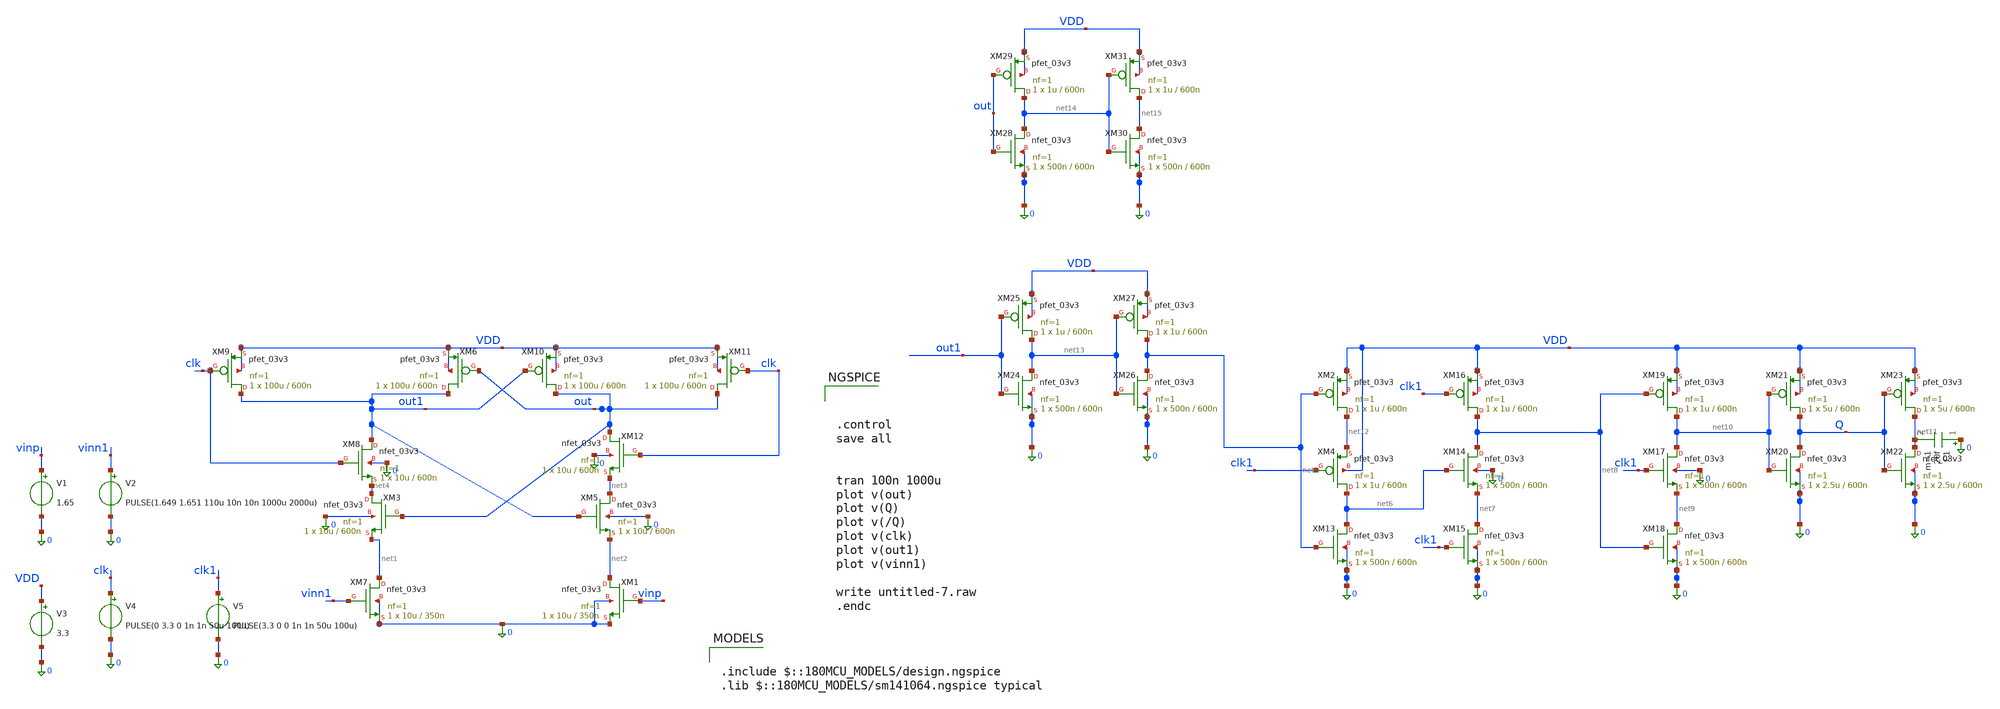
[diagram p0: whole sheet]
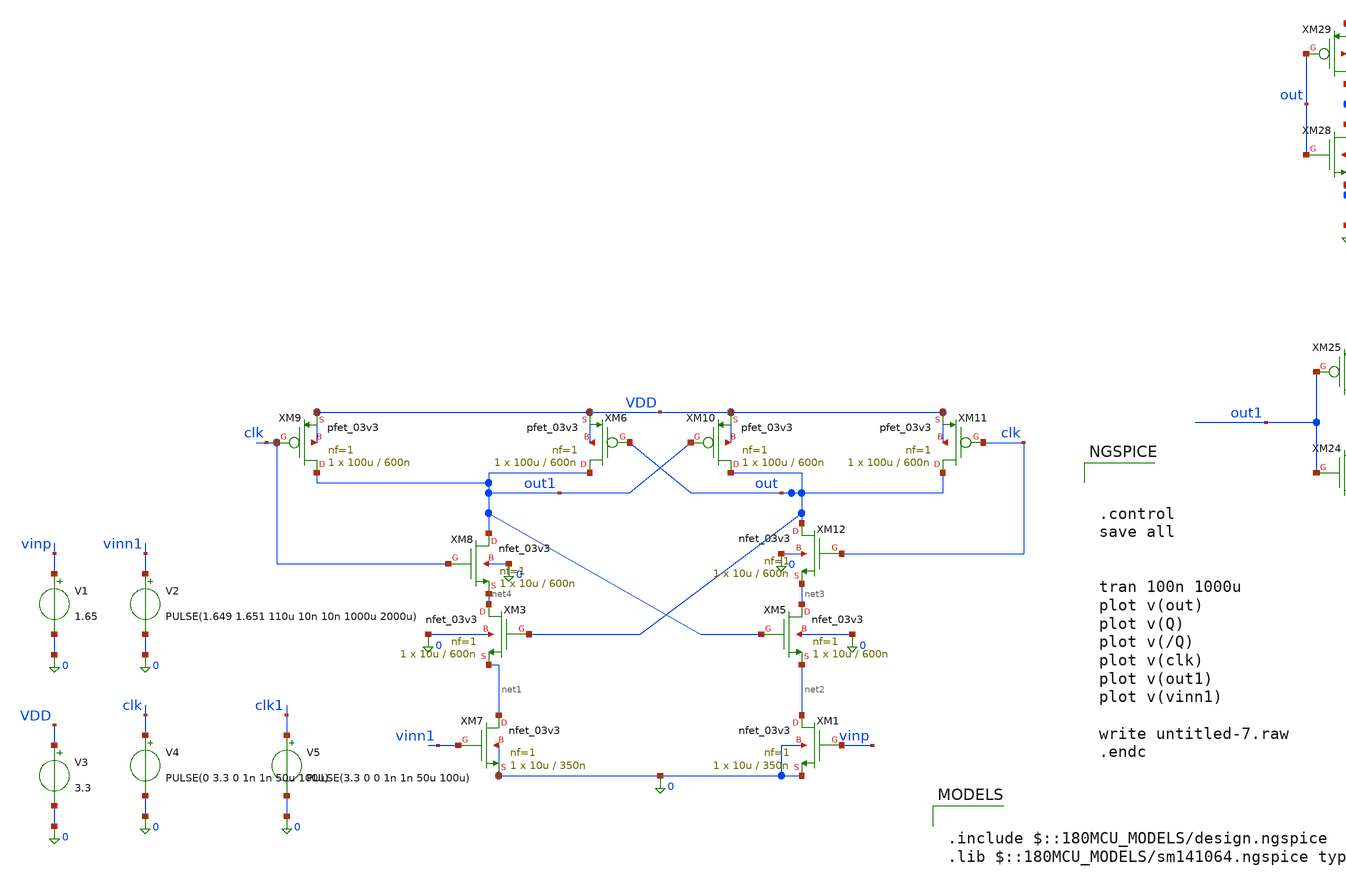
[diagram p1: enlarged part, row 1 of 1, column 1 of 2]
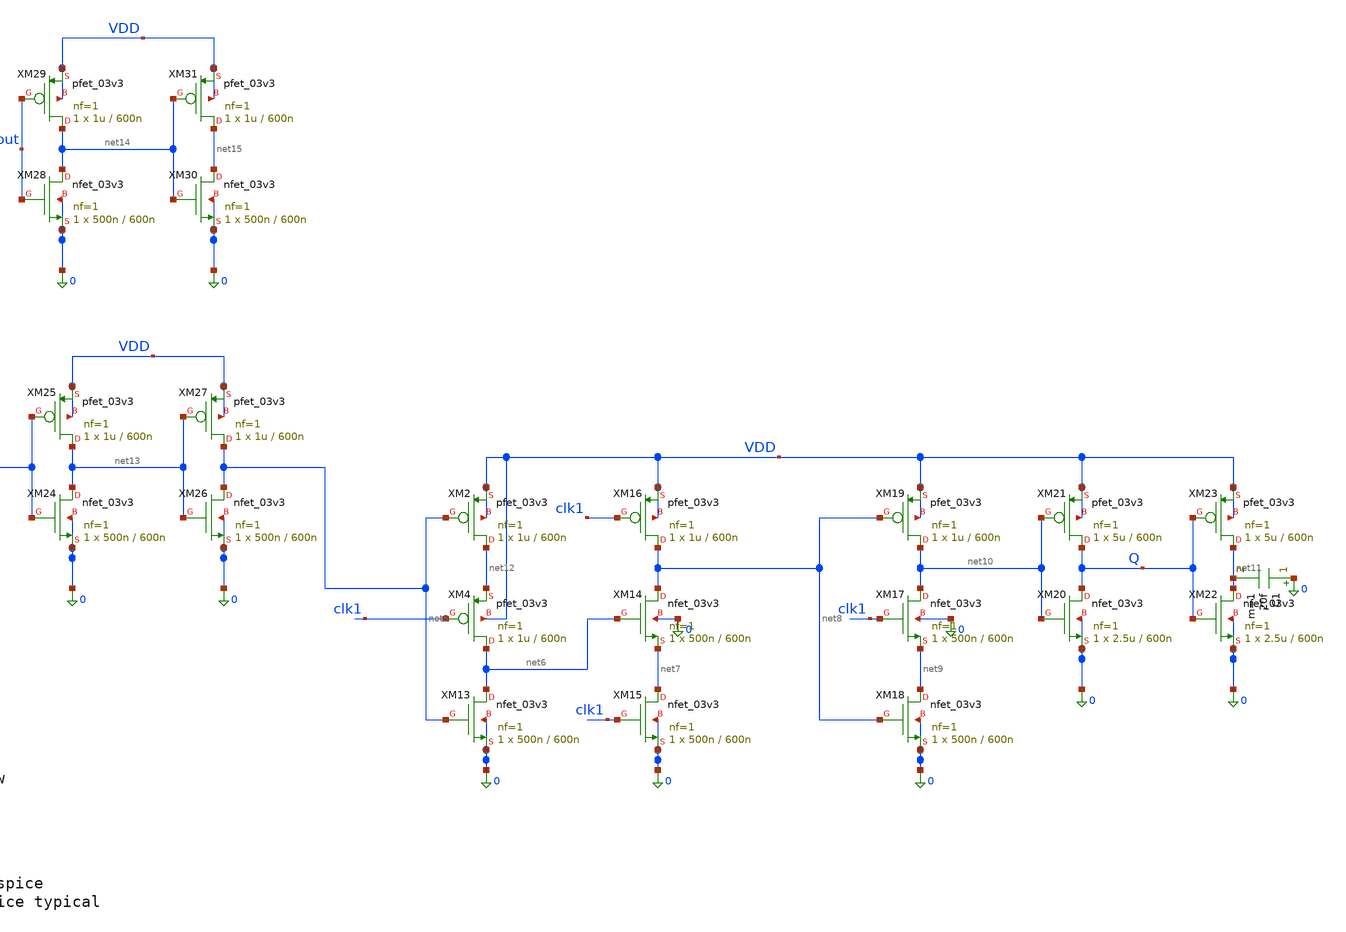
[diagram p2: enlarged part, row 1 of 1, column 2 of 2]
** sch_path: amplifier/untitled-7.sch
**.subckt untitled-7
V1 vinp 0 1.65
V2 vinn1 0 PULSE(1.649 1.651 110u 10n 10n 1000u 2000u)
V3 VDD 0 3.3
XM7 net1 vinn1 0 0 nfet_03v3 L=350n W=10u nf=1 ad='int((nf+1)/2) * W/nf * 0.18u' as='int((nf+2)/2) * W/nf * 0.18u'
+ pd='2*int((nf+1)/2) * (W/nf + 0.18u)' ps='2*int((nf+2)/2) * (W/nf + 0.18u)' nrd='0.18u / W' nrs='0.18u / W'
+ sa=0 sb=0 sd=0 m=1
XM1 net2 vinp 0 0 nfet_03v3 L=350n W=10u nf=1 ad='int((nf+1)/2) * W/nf * 0.18u' as='int((nf+2)/2) * W/nf * 0.18u'
+ pd='2*int((nf+1)/2) * (W/nf + 0.18u)' ps='2*int((nf+2)/2) * (W/nf + 0.18u)' nrd='0.18u / W' nrs='0.18u / W'
+ sa=0 sb=0 sd=0 m=1
XM3 net4 out net1 0 nfet_03v3 L=600n W=10u nf=1 ad='int((nf+1)/2) * W/nf * 0.18u' as='int((nf+2)/2) * W/nf * 0.18u'
+ pd='2*int((nf+1)/2) * (W/nf + 0.18u)' ps='2*int((nf+2)/2) * (W/nf + 0.18u)' nrd='0.18u / W' nrs='0.18u / W'
+ sa=0 sb=0 sd=0 m=1
XM5 net3 out1 net2 0 nfet_03v3 L=600n W=10u nf=1 ad='int((nf+1)/2) * W/nf * 0.18u' as='int((nf+2)/2) * W/nf * 0.18u'
+ pd='2*int((nf+1)/2) * (W/nf + 0.18u)' ps='2*int((nf+2)/2) * (W/nf + 0.18u)' nrd='0.18u / W' nrs='0.18u / W'
+ sa=0 sb=0 sd=0 m=1
V4 clk 0 PULSE(0 3.3 0 1n 1n 50u 100u)
XM6 out1 out VDD VDD pfet_03v3 L=600n W=100u nf=1 ad='int((nf+1)/2) * W/nf * 0.18u' as='int((nf+2)/2) * W/nf * 0.18u'
+ pd='2*int((nf+1)/2) * (W/nf + 0.18u)' ps='2*int((nf+2)/2) * (W/nf + 0.18u)' nrd='0.18u / W' nrs='0.18u / W'
+ sa=0 sb=0 sd=0 m=1
XM10 out out1 VDD VDD pfet_03v3 L=600n W=100u nf=1 ad='int((nf+1)/2) * W/nf * 0.18u' as='int((nf+2)/2) * W/nf * 0.18u'
+ pd='2*int((nf+1)/2) * (W/nf + 0.18u)' ps='2*int((nf+2)/2) * (W/nf + 0.18u)' nrd='0.18u / W' nrs='0.18u / W'
+ sa=0 sb=0 sd=0 m=1
XM9 out1 clk VDD VDD pfet_03v3 L=600n W=100u nf=1 ad='int((nf+1)/2) * W/nf * 0.18u' as='int((nf+2)/2) * W/nf * 0.18u'
+ pd='2*int((nf+1)/2) * (W/nf + 0.18u)' ps='2*int((nf+2)/2) * (W/nf + 0.18u)' nrd='0.18u / W' nrs='0.18u / W'
+ sa=0 sb=0 sd=0 m=1
XM11 out clk VDD VDD pfet_03v3 L=600n W=100u nf=1 ad='int((nf+1)/2) * W/nf * 0.18u' as='int((nf+2)/2) * W/nf * 0.18u'
+ pd='2*int((nf+1)/2) * (W/nf + 0.18u)' ps='2*int((nf+2)/2) * (W/nf + 0.18u)' nrd='0.18u / W' nrs='0.18u / W'
+ sa=0 sb=0 sd=0 m=1
XM8 out1 clk net4 0 nfet_03v3 L=600n W=10u nf=1 ad='int((nf+1)/2) * W/nf * 0.18u' as='int((nf+2)/2) * W/nf * 0.18u'
+ pd='2*int((nf+1)/2) * (W/nf + 0.18u)' ps='2*int((nf+2)/2) * (W/nf + 0.18u)' nrd='0.18u / W' nrs='0.18u / W'
+ sa=0 sb=0 sd=0 m=1
XM12 out clk net3 0 nfet_03v3 L=600n W=10u nf=1 ad='int((nf+1)/2) * W/nf * 0.18u' as='int((nf+2)/2) * W/nf * 0.18u'
+ pd='2*int((nf+1)/2) * (W/nf + 0.18u)' ps='2*int((nf+2)/2) * (W/nf + 0.18u)' nrd='0.18u / W' nrs='0.18u / W'
+ sa=0 sb=0 sd=0 m=1
XM2 net12 net5 VDD VDD pfet_03v3 L=600n W=1u nf=1 ad='int((nf+1)/2) * W/nf * 0.18u' as='int((nf+2)/2) * W/nf * 0.18u'
+ pd='2*int((nf+1)/2) * (W/nf + 0.18u)' ps='2*int((nf+2)/2) * (W/nf + 0.18u)' nrd='0.18u / W' nrs='0.18u / W'
+ sa=0 sb=0 sd=0 m=1
XM4 net6 clk1 net12 VDD pfet_03v3 L=600n W=1u nf=1 ad='int((nf+1)/2) * W/nf * 0.18u' as='int((nf+2)/2) * W/nf * 0.18u'
+ pd='2*int((nf+1)/2) * (W/nf + 0.18u)' ps='2*int((nf+2)/2) * (W/nf + 0.18u)' nrd='0.18u / W' nrs='0.18u / W'
+ sa=0 sb=0 sd=0 m=1
XM13 net6 net5 0 0 nfet_03v3 L=600n W=500n nf=1 ad='int((nf+1)/2) * W/nf * 0.18u' as='int((nf+2)/2) * W/nf * 0.18u'
+ pd='2*int((nf+1)/2) * (W/nf + 0.18u)' ps='2*int((nf+2)/2) * (W/nf + 0.18u)' nrd='0.18u / W' nrs='0.18u / W'
+ sa=0 sb=0 sd=0 m=1
XM14 net8 net6 net7 0 nfet_03v3 L=600n W=500n nf=1 ad='int((nf+1)/2) * W/nf * 0.18u' as='int((nf+2)/2) * W/nf * 0.18u'
+ pd='2*int((nf+1)/2) * (W/nf + 0.18u)' ps='2*int((nf+2)/2) * (W/nf + 0.18u)' nrd='0.18u / W' nrs='0.18u / W'
+ sa=0 sb=0 sd=0 m=1
XM15 net7 clk1 0 0 nfet_03v3 L=600n W=500n nf=1 ad='int((nf+1)/2) * W/nf * 0.18u' as='int((nf+2)/2) * W/nf * 0.18u'
+ pd='2*int((nf+1)/2) * (W/nf + 0.18u)' ps='2*int((nf+2)/2) * (W/nf + 0.18u)' nrd='0.18u / W' nrs='0.18u / W'
+ sa=0 sb=0 sd=0 m=1
XM16 net8 clk1 VDD VDD pfet_03v3 L=600n W=1u nf=1 ad='int((nf+1)/2) * W/nf * 0.18u' as='int((nf+2)/2) * W/nf * 0.18u'
+ pd='2*int((nf+1)/2) * (W/nf + 0.18u)' ps='2*int((nf+2)/2) * (W/nf + 0.18u)' nrd='0.18u / W' nrs='0.18u / W'
+ sa=0 sb=0 sd=0 m=1
XM17 net10 clk1 net9 0 nfet_03v3 L=600n W=500n nf=1 ad='int((nf+1)/2) * W/nf * 0.18u' as='int((nf+2)/2) * W/nf * 0.18u'
+ pd='2*int((nf+1)/2) * (W/nf + 0.18u)' ps='2*int((nf+2)/2) * (W/nf + 0.18u)' nrd='0.18u / W' nrs='0.18u / W'
+ sa=0 sb=0 sd=0 m=1
XM18 net9 net8 0 0 nfet_03v3 L=600n W=500n nf=1 ad='int((nf+1)/2) * W/nf * 0.18u' as='int((nf+2)/2) * W/nf * 0.18u'
+ pd='2*int((nf+1)/2) * (W/nf + 0.18u)' ps='2*int((nf+2)/2) * (W/nf + 0.18u)' nrd='0.18u / W' nrs='0.18u / W'
+ sa=0 sb=0 sd=0 m=1
XM19 net10 net8 VDD VDD pfet_03v3 L=600n W=1u nf=1 ad='int((nf+1)/2) * W/nf * 0.18u' as='int((nf+2)/2) * W/nf * 0.18u'
+ pd='2*int((nf+1)/2) * (W/nf + 0.18u)' ps='2*int((nf+2)/2) * (W/nf + 0.18u)' nrd='0.18u / W' nrs='0.18u / W'
+ sa=0 sb=0 sd=0 m=1
XM20 Q net10 0 0 nfet_03v3 L=600n W=2.5u nf=1 ad='int((nf+1)/2) * W/nf * 0.18u' as='int((nf+2)/2) * W/nf * 0.18u'
+ pd='2*int((nf+1)/2) * (W/nf + 0.18u)' ps='2*int((nf+2)/2) * (W/nf + 0.18u)' nrd='0.18u / W' nrs='0.18u / W'
+ sa=0 sb=0 sd=0 m=1
XM21 Q net10 VDD VDD pfet_03v3 L=600n W=5u nf=1 ad='int((nf+1)/2) * W/nf * 0.18u' as='int((nf+2)/2) * W/nf * 0.18u'
+ pd='2*int((nf+1)/2) * (W/nf + 0.18u)' ps='2*int((nf+2)/2) * (W/nf + 0.18u)' nrd='0.18u / W' nrs='0.18u / W'
+ sa=0 sb=0 sd=0 m=1
XM22 net11 Q 0 0 nfet_03v3 L=600n W=2.5u nf=1 ad='int((nf+1)/2) * W/nf * 0.18u' as='int((nf+2)/2) * W/nf * 0.18u'
+ pd='2*int((nf+1)/2) * (W/nf + 0.18u)' ps='2*int((nf+2)/2) * (W/nf + 0.18u)' nrd='0.18u / W' nrs='0.18u / W'
+ sa=0 sb=0 sd=0 m=1
XM23 net11 Q VDD VDD pfet_03v3 L=600n W=5u nf=1 ad='int((nf+1)/2) * W/nf * 0.18u' as='int((nf+2)/2) * W/nf * 0.18u'
+ pd='2*int((nf+1)/2) * (W/nf + 0.18u)' ps='2*int((nf+2)/2) * (W/nf + 0.18u)' nrd='0.18u / W' nrs='0.18u / W'
+ sa=0 sb=0 sd=0 m=1
V5 clk1 0 PULSE(3.3 0 0 1n 1n 50u 100u)
C1 0 net11 20f m=1
XM24 net13 out1 0 0 nfet_03v3 L=600n W=500n nf=1 ad='int((nf+1)/2) * W/nf * 0.18u' as='int((nf+2)/2) * W/nf * 0.18u'
+ pd='2*int((nf+1)/2) * (W/nf + 0.18u)' ps='2*int((nf+2)/2) * (W/nf + 0.18u)' nrd='0.18u / W' nrs='0.18u / W'
+ sa=0 sb=0 sd=0 m=1
XM25 net13 out1 VDD VDD pfet_03v3 L=600n W=1u nf=1 ad='int((nf+1)/2) * W/nf * 0.18u' as='int((nf+2)/2) * W/nf * 0.18u'
+ pd='2*int((nf+1)/2) * (W/nf + 0.18u)' ps='2*int((nf+2)/2) * (W/nf + 0.18u)' nrd='0.18u / W' nrs='0.18u / W'
+ sa=0 sb=0 sd=0 m=1
XM26 net5 net13 0 0 nfet_03v3 L=600n W=500n nf=1 ad='int((nf+1)/2) * W/nf * 0.18u' as='int((nf+2)/2) * W/nf * 0.18u'
+ pd='2*int((nf+1)/2) * (W/nf + 0.18u)' ps='2*int((nf+2)/2) * (W/nf + 0.18u)' nrd='0.18u / W' nrs='0.18u / W'
+ sa=0 sb=0 sd=0 m=1
XM27 net5 net13 VDD VDD pfet_03v3 L=600n W=1u nf=1 ad='int((nf+1)/2) * W/nf * 0.18u' as='int((nf+2)/2) * W/nf * 0.18u'
+ pd='2*int((nf+1)/2) * (W/nf + 0.18u)' ps='2*int((nf+2)/2) * (W/nf + 0.18u)' nrd='0.18u / W' nrs='0.18u / W'
+ sa=0 sb=0 sd=0 m=1
XM28 net14 out 0 0 nfet_03v3 L=600n W=500n nf=1 ad='int((nf+1)/2) * W/nf * 0.18u' as='int((nf+2)/2) * W/nf * 0.18u'
+ pd='2*int((nf+1)/2) * (W/nf + 0.18u)' ps='2*int((nf+2)/2) * (W/nf + 0.18u)' nrd='0.18u / W' nrs='0.18u / W'
+ sa=0 sb=0 sd=0 m=1
XM29 net14 out VDD VDD pfet_03v3 L=600n W=1u nf=1 ad='int((nf+1)/2) * W/nf * 0.18u' as='int((nf+2)/2) * W/nf * 0.18u'
+ pd='2*int((nf+1)/2) * (W/nf + 0.18u)' ps='2*int((nf+2)/2) * (W/nf + 0.18u)' nrd='0.18u / W' nrs='0.18u / W'
+ sa=0 sb=0 sd=0 m=1
XM30 net15 net14 0 0 nfet_03v3 L=600n W=500n nf=1 ad='int((nf+1)/2) * W/nf * 0.18u' as='int((nf+2)/2) * W/nf * 0.18u'
+ pd='2*int((nf+1)/2) * (W/nf + 0.18u)' ps='2*int((nf+2)/2) * (W/nf + 0.18u)' nrd='0.18u / W' nrs='0.18u / W'
+ sa=0 sb=0 sd=0 m=1
XM31 net15 net14 VDD VDD pfet_03v3 L=600n W=1u nf=1 ad='int((nf+1)/2) * W/nf * 0.18u' as='int((nf+2)/2) * W/nf * 0.18u'
+ pd='2*int((nf+1)/2) * (W/nf + 0.18u)' ps='2*int((nf+2)/2) * (W/nf + 0.18u)' nrd='0.18u / W' nrs='0.18u / W'
+ sa=0 sb=0 sd=0 m=1
**** begin user architecture code



.control
save all


tran 100n 1000u
plot v(out)
plot v(Q)
plot v(/Q)
plot v(clk)
plot v(out1)
plot v(vinn1)

write untitled-7.raw
.endc



.include $::180MCU_MODELS/design.ngspice
.lib $::180MCU_MODELS/sm141064.ngspice typical

**** end user architecture code
**.ends
.end
